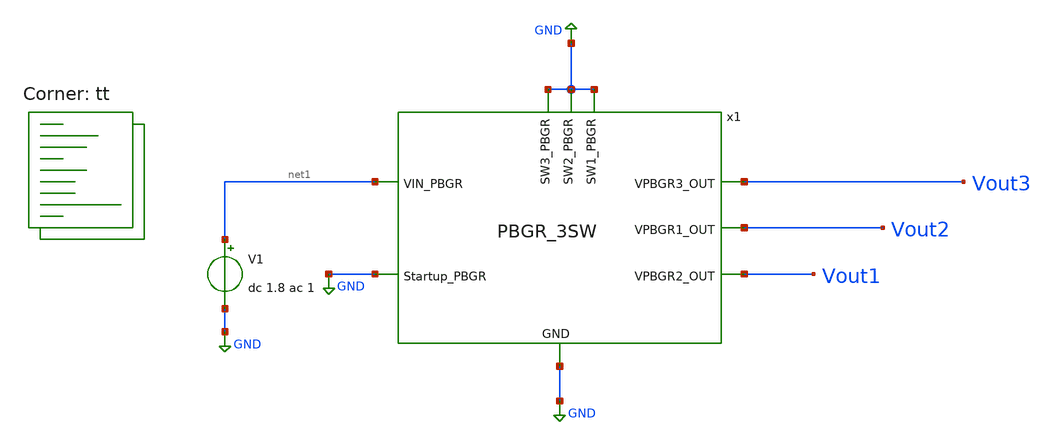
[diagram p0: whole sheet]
** sch_path: PBGR/Three_switch_BGR/tb-try2.sch
**.subckt tb-try2
V1 net1 GND dc 1.8 ac 1
x1 net1 GND Vout3 Vout2 Vout1 GND GND GND GND PBGR_3SW
**** begin user architecture code
.lib $::SKYWATER_MODELS/sky130.lib.spice tt


.option wnflag=1
.option savecurrents
.temp 27
.control
save all
write tb-try2.raw
set appendwrite
op
write tb-try2.raw
dc temp -50 150 1
**ac dec 20 1 1e8
plot v(Vout1) v(Vout2) v(Vout3)
plot v(Vout1)
plot v(Vout2)
plot v(Vout3)
plot vdb(Vout1) vdb(Vout2) vdb(Vout3)
.endc


**** end user architecture code
**.ends

* expanding   symbol:  /foss/designs/Sims-new/PBGR/Final-submission/PBGR_3SW.sym # of pins=9
** sym_path: PBGR/Three_switch_BGR/PBGR_3SW.sym
** sch_path: PBGR/Three_switch_BGR/PBGR_3SW.sch
.subckt PBGR_3SW VIN_PBGR Startup_PBGR VPBGR3_OUT VPBGR1_OUT VPBGR2_OUT SW1_PBGR SW2_PBGR SW3_PBGR
+ GND
*.opin VPBGR3_OUT
*.opin VPBGR2_OUT
*.opin VPBGR1_OUT
*.ipin VIN_PBGR
*.ipin GND
*.ipin Startup_PBGR
*.ipin SW1_PBGR
*.ipin SW2_PBGR
*.ipin SW3_PBGR
XM1 net1 vctrl VIN_PBGR VIN_PBGR sky130_fd_pr__pfet_01v8 L=3 W=6.75 nf=1 ad='int((nf+1)/2) * W/nf * 0.29'
+ as='int((nf+2)/2) * W/nf * 0.29' pd='2*int((nf+1)/2) * (W/nf + 0.29)' ps='2*int((nf+2)/2) * (W/nf + 0.29)'
+ nrd='0.29 / W' nrs='0.29 / W' sa=0 sb=0 sd=0 mult=4 m=4
XM2 minus vb0 net1 VIN_PBGR sky130_fd_pr__pfet_01v8 L=3 W=6.75 nf=1 ad='int((nf+1)/2) * W/nf * 0.29'
+ as='int((nf+2)/2) * W/nf * 0.29' pd='2*int((nf+1)/2) * (W/nf + 0.29)' ps='2*int((nf+2)/2) * (W/nf + 0.29)'
+ nrd='0.29 / W' nrs='0.29 / W' sa=0 sb=0 sd=0 mult=4 m=4
XM3 net2 vctrl VIN_PBGR VIN_PBGR sky130_fd_pr__pfet_01v8 L=3 W=6.75 nf=1 ad='int((nf+1)/2) * W/nf * 0.29'
+ as='int((nf+2)/2) * W/nf * 0.29' pd='2*int((nf+1)/2) * (W/nf + 0.29)' ps='2*int((nf+2)/2) * (W/nf + 0.29)'
+ nrd='0.29 / W' nrs='0.29 / W' sa=0 sb=0 sd=0 mult=4 m=4
XM4 plus vb0 net2 VIN_PBGR sky130_fd_pr__pfet_01v8 L=3 W=6.75 nf=1 ad='int((nf+1)/2) * W/nf * 0.29' as='int((nf+2)/2) * W/nf * 0.29'
+ pd='2*int((nf+1)/2) * (W/nf + 0.29)' ps='2*int((nf+2)/2) * (W/nf + 0.29)' nrd='0.29 / W' nrs='0.29 / W'
+ sa=0 sb=0 sd=0 mult=4 m=4
XR1 net29 plus GND sky130_fd_pr__res_xhigh_po_1p41 L=2.262 mult=1 m=1
XR2 net30 net29 GND sky130_fd_pr__res_xhigh_po_1p41 L=2.262 mult=1 m=1
XR3 net31 net30 GND sky130_fd_pr__res_xhigh_po_1p41 L=2.262 mult=1 m=1
XR4 net3 net31 GND sky130_fd_pr__res_xhigh_po_1p41 L=2.262 mult=1 m=1
XQ1 GND GND net3 sky130_fd_pr__pnp_05v5_W3p40L3p40 m=8
XQ2 GND GND minus sky130_fd_pr__pnp_05v5_W3p40L3p40 m=1
XR5 net32 plus GND sky130_fd_pr__res_xhigh_po_1p41 L=21.11 mult=1 m=1
XR6 net33 net32 GND sky130_fd_pr__res_xhigh_po_1p41 L=21.11 mult=1 m=1
XR7 net34 net33 GND sky130_fd_pr__res_xhigh_po_1p41 L=21.11 mult=1 m=1
XR8 GND net34 GND sky130_fd_pr__res_xhigh_po_1p41 L=21.11 mult=1 m=1
XR9 net35 minus GND sky130_fd_pr__res_xhigh_po_1p41 L=21.11 mult=1 m=1
XR10 net36 net35 GND sky130_fd_pr__res_xhigh_po_1p41 L=21.11 mult=1 m=1
XR11 net37 net36 GND sky130_fd_pr__res_xhigh_po_1p41 L=21.11 mult=1 m=1
XR12 GND net37 GND sky130_fd_pr__res_xhigh_po_1p41 L=21.11 mult=1 m=1
XM7 net4 vctrl VIN_PBGR VIN_PBGR sky130_fd_pr__pfet_01v8 L=3 W=6.75 nf=1 ad='int((nf+1)/2) * W/nf * 0.29'
+ as='int((nf+2)/2) * W/nf * 0.29' pd='2*int((nf+1)/2) * (W/nf + 0.29)' ps='2*int((nf+2)/2) * (W/nf + 0.29)'
+ nrd='0.29 / W' nrs='0.29 / W' sa=0 sb=0 sd=0 mult=4 m=4
XM8 net5 vb0 net4 VIN_PBGR sky130_fd_pr__pfet_01v8 L=3 W=6.75 nf=1 ad='int((nf+1)/2) * W/nf * 0.29' as='int((nf+2)/2) * W/nf * 0.29'
+ pd='2*int((nf+1)/2) * (W/nf + 0.29)' ps='2*int((nf+2)/2) * (W/nf + 0.29)' nrd='0.29 / W' nrs='0.29 / W'
+ sa=0 sb=0 sd=0 mult=4 m=4
XR21 net38 net5 GND sky130_fd_pr__res_xhigh_po_1p41 L=3.7 mult=1 m=1
XM9 net6 net5 GND GND sky130_fd_pr__nfet_01v8_lvt L=0.15 W=1 nf=1 ad='int((nf+1)/2) * W/nf * 0.29' as='int((nf+2)/2) * W/nf * 0.29'
+ pd='2*int((nf+1)/2) * (W/nf + 0.29)' ps='2*int((nf+2)/2) * (W/nf + 0.29)' nrd='0.29 / W' nrs='0.29 / W'
+ sa=0 sb=0 sd=0 mult=1 m=1
XM10 net6 net6 VIN_PBGR VIN_PBGR sky130_fd_pr__pfet_01v8 L=3 W=6.75 nf=1 ad='int((nf+1)/2) * W/nf * 0.29'
+ as='int((nf+2)/2) * W/nf * 0.29' pd='2*int((nf+1)/2) * (W/nf + 0.29)' ps='2*int((nf+2)/2) * (W/nf + 0.29)'
+ nrd='0.29 / W' nrs='0.29 / W' sa=0 sb=0 sd=0 mult=4 m=4
XM11 VPBGR1_OUT net6 VIN_PBGR VIN_PBGR sky130_fd_pr__pfet_01v8 L=3 W=6.75 nf=1 ad='int((nf+1)/2) * W/nf * 0.29'
+ as='int((nf+2)/2) * W/nf * 0.29' pd='2*int((nf+1)/2) * (W/nf + 0.29)' ps='2*int((nf+2)/2) * (W/nf + 0.29)'
+ nrd='0.29 / W' nrs='0.29 / W' sa=0 sb=0 sd=0 mult=4 m=4
XM12 net7 vctrl VIN_PBGR VIN_PBGR sky130_fd_pr__pfet_01v8 L=3 W=6.75 nf=1 ad='int((nf+1)/2) * W/nf * 0.29'
+ as='int((nf+2)/2) * W/nf * 0.29' pd='2*int((nf+1)/2) * (W/nf + 0.29)' ps='2*int((nf+2)/2) * (W/nf + 0.29)'
+ nrd='0.29 / W' nrs='0.29 / W' sa=0 sb=0 sd=0 mult=4 m=4
XM13 VPBGR1_OUT vb0 net7 VIN_PBGR sky130_fd_pr__pfet_01v8 L=3 W=6.75 nf=1 ad='int((nf+1)/2) * W/nf * 0.29'
+ as='int((nf+2)/2) * W/nf * 0.29' pd='2*int((nf+1)/2) * (W/nf + 0.29)' ps='2*int((nf+2)/2) * (W/nf + 0.29)'
+ nrd='0.29 / W' nrs='0.29 / W' sa=0 sb=0 sd=0 mult=4 m=4
XR27 net39 VPBGR1_OUT GND sky130_fd_pr__res_xhigh_po_1p41 L=5.61 mult=1 m=1
XR28 net40 net39 GND sky130_fd_pr__res_xhigh_po_1p41 L=5.61 mult=1 m=1
XR29 net41 net40 GND sky130_fd_pr__res_xhigh_po_1p41 L=5.61 mult=1 m=1
XR30 net42 net41 GND sky130_fd_pr__res_xhigh_po_1p41 L=5.61 mult=1 m=1
XR31 net43 net42 GND sky130_fd_pr__res_xhigh_po_1p41 L=5.61 mult=1 m=1
XR32 net44 net43 GND sky130_fd_pr__res_xhigh_po_1p41 L=5.61 mult=1 m=1
XR33 net45 net44 GND sky130_fd_pr__res_xhigh_po_1p41 L=5.61 mult=1 m=1
XR34 GND net45 GND sky130_fd_pr__res_xhigh_po_1p41 L=5.61 mult=1 m=1
XM14 net8 vctrl VIN_PBGR VIN_PBGR sky130_fd_pr__pfet_01v8 L=3 W=5.4 nf=1 ad='int((nf+1)/2) * W/nf * 0.29'
+ as='int((nf+2)/2) * W/nf * 0.29' pd='2*int((nf+1)/2) * (W/nf + 0.29)' ps='2*int((nf+2)/2) * (W/nf + 0.29)'
+ nrd='0.29 / W' nrs='0.29 / W' sa=0 sb=0 sd=0 mult=1 m=1
XR36 net46 net9 GND sky130_fd_pr__res_xhigh_po_1p41 L=18 mult=1 m=1
XM16 net10 net9 GND GND sky130_fd_pr__nfet_01v8_lvt L=0.15 W=1 nf=1 ad='int((nf+1)/2) * W/nf * 0.29'
+ as='int((nf+2)/2) * W/nf * 0.29' pd='2*int((nf+1)/2) * (W/nf + 0.29)' ps='2*int((nf+2)/2) * (W/nf + 0.29)'
+ nrd='0.29 / W' nrs='0.29 / W' sa=0 sb=0 sd=0 mult=1 m=1
XM17 net10 net10 VIN_PBGR VIN_PBGR sky130_fd_pr__pfet_01v8 L=3 W=6.75 nf=1 ad='int((nf+1)/2) * W/nf * 0.29'
+ as='int((nf+2)/2) * W/nf * 0.29' pd='2*int((nf+1)/2) * (W/nf + 0.29)' ps='2*int((nf+2)/2) * (W/nf + 0.29)'
+ nrd='0.29 / W' nrs='0.29 / W' sa=0 sb=0 sd=0 mult=4 m=4
XM18 VPBGR2_OUT net10 VIN_PBGR VIN_PBGR sky130_fd_pr__pfet_01v8 L=3 W=6.75 nf=1 ad='int((nf+1)/2) * W/nf * 0.29'
+ as='int((nf+2)/2) * W/nf * 0.29' pd='2*int((nf+1)/2) * (W/nf + 0.29)' ps='2*int((nf+2)/2) * (W/nf + 0.29)'
+ nrd='0.29 / W' nrs='0.29 / W' sa=0 sb=0 sd=0 mult=4 m=4
XM19 net11 vctrl VIN_PBGR VIN_PBGR sky130_fd_pr__pfet_01v8 L=3 W=6.75 nf=1 ad='int((nf+1)/2) * W/nf * 0.29'
+ as='int((nf+2)/2) * W/nf * 0.29' pd='2*int((nf+1)/2) * (W/nf + 0.29)' ps='2*int((nf+2)/2) * (W/nf + 0.29)'
+ nrd='0.29 / W' nrs='0.29 / W' sa=0 sb=0 sd=0 mult=4 m=4
XM20 VPBGR2_OUT vb0 net11 VIN_PBGR sky130_fd_pr__pfet_01v8 L=3 W=6.75 nf=1 ad='int((nf+1)/2) * W/nf * 0.29'
+ as='int((nf+2)/2) * W/nf * 0.29' pd='2*int((nf+1)/2) * (W/nf + 0.29)' ps='2*int((nf+2)/2) * (W/nf + 0.29)'
+ nrd='0.29 / W' nrs='0.29 / W' sa=0 sb=0 sd=0 mult=4 m=4
XR41 net47 VPBGR2_OUT GND sky130_fd_pr__res_xhigh_po_1p41 L=5.61 mult=1 m=1
XR42 net48 net47 GND sky130_fd_pr__res_xhigh_po_1p41 L=5.61 mult=1 m=1
XR43 net49 net48 GND sky130_fd_pr__res_xhigh_po_1p41 L=5.61 mult=1 m=1
XR44 net50 net49 GND sky130_fd_pr__res_xhigh_po_1p41 L=5.61 mult=1 m=1
XR45 net51 net50 GND sky130_fd_pr__res_xhigh_po_1p41 L=5.61 mult=1 m=1
XR46 net52 net51 GND sky130_fd_pr__res_xhigh_po_1p41 L=5.61 mult=1 m=1
XR47 net53 net52 GND sky130_fd_pr__res_xhigh_po_1p41 L=5.61 mult=1 m=1
XR48 GND net53 GND sky130_fd_pr__res_xhigh_po_1p41 L=5.61 mult=1 m=1
XR35 net54 net46 GND sky130_fd_pr__res_xhigh_po_1p41 L=18 mult=1 m=1
XR37 GND net55 GND sky130_fd_pr__res_xhigh_po_1p41 L=18 mult=1 m=1
XR38 net55 net54 GND sky130_fd_pr__res_xhigh_po_1p41 L=18 mult=1 m=1
XM15 net9 vb0 net8 VIN_PBGR sky130_fd_pr__pfet_01v8 L=3 W=5.4 nf=1 ad='int((nf+1)/2) * W/nf * 0.29' as='int((nf+2)/2) * W/nf * 0.29'
+ pd='2*int((nf+1)/2) * (W/nf + 0.29)' ps='2*int((nf+2)/2) * (W/nf + 0.29)' nrd='0.29 / W' nrs='0.29 / W'
+ sa=0 sb=0 sd=0 mult=1 m=1
.save v(plus)
.save v(minus)
XM21 vb0 vb0 VIN_PBGR VIN_PBGR sky130_fd_pr__pfet_01v8 L=3 W=6.75 nf=1 ad='int((nf+1)/2) * W/nf * 0.29'
+ as='int((nf+2)/2) * W/nf * 0.29' pd='2*int((nf+1)/2) * (W/nf + 0.29)' ps='2*int((nf+2)/2) * (W/nf + 0.29)'
+ nrd='0.29 / W' nrs='0.29 / W' sa=0 sb=0 sd=0 mult=1 m=1
XR26 net56 vb0 GND sky130_fd_pr__res_xhigh_po_1p41 L=2.9 mult=1 m=1
XR39 net57 net56 GND sky130_fd_pr__res_xhigh_po_1p41 L=2.9 mult=1 m=1
XR40 net58 net57 GND sky130_fd_pr__res_xhigh_po_1p41 L=2.9 mult=1 m=1
XR49 net59 net58 GND sky130_fd_pr__res_xhigh_po_1p41 L=2.9 mult=1 m=1
XR50 net60 net59 GND sky130_fd_pr__res_xhigh_po_1p41 L=2.9 mult=1 m=1
XR51 net61 net60 GND sky130_fd_pr__res_xhigh_po_1p41 L=2.9 mult=1 m=1
XR52 net62 net61 GND sky130_fd_pr__res_xhigh_po_1p41 L=2.9 mult=1 m=1
XR53 GND net62 GND sky130_fd_pr__res_xhigh_po_1p41 L=2.9 mult=1 m=1
XR22 net63 net38 GND sky130_fd_pr__res_xhigh_po_1p41 L=3.7 mult=1 m=1
XR23 GND net64 GND sky130_fd_pr__res_xhigh_po_1p41 L=3.7 mult=1 m=1
XR24 net64 net63 GND sky130_fd_pr__res_xhigh_po_1p41 L=3.7 mult=1 m=1
XM5 net13 minus net12 GND sky130_fd_pr__nfet_01v8_lvt L=1.5 W=2.25 nf=1 ad='int((nf+1)/2) * W/nf * 0.29'
+ as='int((nf+2)/2) * W/nf * 0.29' pd='2*int((nf+1)/2) * (W/nf + 0.29)' ps='2*int((nf+2)/2) * (W/nf + 0.29)'
+ nrd='0.29 / W' nrs='0.29 / W' sa=0 sb=0 sd=0 mult=4 m=4
XM6 net14 plus net12 GND sky130_fd_pr__nfet_01v8_lvt L=1.5 W=2.25 nf=1 ad='int((nf+1)/2) * W/nf * 0.29'
+ as='int((nf+2)/2) * W/nf * 0.29' pd='2*int((nf+1)/2) * (W/nf + 0.29)' ps='2*int((nf+2)/2) * (W/nf + 0.29)'
+ nrd='0.29 / W' nrs='0.29 / W' sa=0 sb=0 sd=0 mult=4 m=4
XM22 net12 net15 GND GND sky130_fd_pr__nfet_01v8 L=2.5 W=2 nf=1 ad='int((nf+1)/2) * W/nf * 0.29' as='int((nf+2)/2) * W/nf * 0.29'
+ pd='2*int((nf+1)/2) * (W/nf + 0.29)' ps='2*int((nf+2)/2) * (W/nf + 0.29)' nrd='0.29 / W' nrs='0.29 / W'
+ sa=0 sb=0 sd=0 mult=4 m=4
XM23 net13 net13 VIN_PBGR VIN_PBGR sky130_fd_pr__pfet_01v8 L=1 W=3 nf=1 ad='int((nf+1)/2) * W/nf * 0.29'
+ as='int((nf+2)/2) * W/nf * 0.29' pd='2*int((nf+1)/2) * (W/nf + 0.29)' ps='2*int((nf+2)/2) * (W/nf + 0.29)'
+ nrd='0.29 / W' nrs='0.29 / W' sa=0 sb=0 sd=0 mult=1 m=1
XM24 net14 net13 VIN_PBGR VIN_PBGR sky130_fd_pr__pfet_01v8 L=1 W=3 nf=1 ad='int((nf+1)/2) * W/nf * 0.29'
+ as='int((nf+2)/2) * W/nf * 0.29' pd='2*int((nf+1)/2) * (W/nf + 0.29)' ps='2*int((nf+2)/2) * (W/nf + 0.29)'
+ nrd='0.29 / W' nrs='0.29 / W' sa=0 sb=0 sd=0 mult=1 m=1
XM25 net15 net15 GND GND sky130_fd_pr__nfet_01v8 L=2.5 W=2 nf=1 ad='int((nf+1)/2) * W/nf * 0.29' as='int((nf+2)/2) * W/nf * 0.29'
+ pd='2*int((nf+1)/2) * (W/nf + 0.29)' ps='2*int((nf+2)/2) * (W/nf + 0.29)' nrd='0.29 / W' nrs='0.29 / W'
+ sa=0 sb=0 sd=0 mult=4 m=4
XR13 net15 net65 GND sky130_fd_pr__res_xhigh_po_1p41 L=9 mult=1 m=1
XR14 net65 net66 GND sky130_fd_pr__res_xhigh_po_1p41 L=9 mult=1 m=1
XR15 net66 net67 GND sky130_fd_pr__res_xhigh_po_1p41 L=9 mult=1 m=1
XR16 net67 net68 GND sky130_fd_pr__res_xhigh_po_1p41 L=9 mult=1 m=1
XR17 net68 net16 GND sky130_fd_pr__res_xhigh_po_1p41 L=9 mult=1 m=1
XR18 net17 net69 GND sky130_fd_pr__res_xhigh_po_1p41 L=9 mult=1 m=1
XR19 net69 net70 GND sky130_fd_pr__res_xhigh_po_1p41 L=9 mult=1 m=1
XR20 net70 net71 GND sky130_fd_pr__res_xhigh_po_1p41 L=9 mult=1 m=1
XR59 net71 net72 GND sky130_fd_pr__res_xhigh_po_1p41 L=9 mult=1 m=1
XR60 net72 net16 GND sky130_fd_pr__res_xhigh_po_1p41 L=9 mult=1 m=1
XR61 net17 net73 GND sky130_fd_pr__res_xhigh_po_1p41 L=9 mult=1 m=1
XR62 net73 net74 GND sky130_fd_pr__res_xhigh_po_1p41 L=9 mult=1 m=1
XR63 net74 net75 GND sky130_fd_pr__res_xhigh_po_1p41 L=9 mult=1 m=1
XR64 net75 net76 GND sky130_fd_pr__res_xhigh_po_1p41 L=9 mult=1 m=1
XR65 net76 net77 GND sky130_fd_pr__res_xhigh_po_1p41 L=9 mult=1 m=1
XR66 net77 VIN_PBGR GND sky130_fd_pr__res_xhigh_po_1p41 L=9 mult=1 m=1
XM26 vctrl net15 GND GND sky130_fd_pr__nfet_01v8 L=2.5 W=8 nf=1 ad='int((nf+1)/2) * W/nf * 0.29' as='int((nf+2)/2) * W/nf * 0.29'
+ pd='2*int((nf+1)/2) * (W/nf + 0.29)' ps='2*int((nf+2)/2) * (W/nf + 0.29)' nrd='0.29 / W' nrs='0.29 / W'
+ sa=0 sb=0 sd=0 mult=4 m=4
XM27 vctrl net14 VIN_PBGR VIN_PBGR sky130_fd_pr__pfet_01v8 L=1 W=4.25 nf=1 ad='int((nf+1)/2) * W/nf * 0.29'
+ as='int((nf+2)/2) * W/nf * 0.29' pd='2*int((nf+1)/2) * (W/nf + 0.29)' ps='2*int((nf+2)/2) * (W/nf + 0.29)'
+ nrd='0.29 / W' nrs='0.29 / W' sa=0 sb=0 sd=0 mult=8 m=8
XR67 net18 vctrl GND sky130_fd_pr__res_xhigh_po_1p41 L=3.5 mult=1 m=1
XC1 net14 net18 sky130_fd_pr__cap_mim_m3_1 W=9.75 L=9.75 MF=8 m=8
XM28 net19 vctrl VIN_PBGR VIN_PBGR sky130_fd_pr__pfet_01v8 L=3 W=6.75 nf=1 ad='int((nf+1)/2) * W/nf * 0.29'
+ as='int((nf+2)/2) * W/nf * 0.29' pd='2*int((nf+1)/2) * (W/nf + 0.29)' ps='2*int((nf+2)/2) * (W/nf + 0.29)'
+ nrd='0.29 / W' nrs='0.29 / W' sa=0 sb=0 sd=0 mult=4 m=4
XM29 net20 vb0 net19 VIN_PBGR sky130_fd_pr__pfet_01v8 L=3 W=6.75 nf=1 ad='int((nf+1)/2) * W/nf * 0.29'
+ as='int((nf+2)/2) * W/nf * 0.29' pd='2*int((nf+1)/2) * (W/nf + 0.29)' ps='2*int((nf+2)/2) * (W/nf + 0.29)'
+ nrd='0.29 / W' nrs='0.29 / W' sa=0 sb=0 sd=0 mult=4 m=4
XR68 net78 net20 GND sky130_fd_pr__res_xhigh_po_1p41 L=4.15 mult=1 m=1
XR69 net79 net78 GND sky130_fd_pr__res_xhigh_po_1p41 L=4.15 mult=1 m=1
XR70 net80 net79 GND sky130_fd_pr__res_xhigh_po_1p41 L=4.15 mult=1 m=1
XR71 GND net80 GND sky130_fd_pr__res_xhigh_po_1p41 L=4.15 mult=1 m=1
XM30 net21 net20 GND GND sky130_fd_pr__nfet_01v8_lvt L=0.15 W=1 nf=1 ad='int((nf+1)/2) * W/nf * 0.29'
+ as='int((nf+2)/2) * W/nf * 0.29' pd='2*int((nf+1)/2) * (W/nf + 0.29)' ps='2*int((nf+2)/2) * (W/nf + 0.29)'
+ nrd='0.29 / W' nrs='0.29 / W' sa=0 sb=0 sd=0 mult=1 m=1
XM31 net21 net21 VIN_PBGR VIN_PBGR sky130_fd_pr__pfet_01v8 L=3 W=6.75 nf=1 ad='int((nf+1)/2) * W/nf * 0.29'
+ as='int((nf+2)/2) * W/nf * 0.29' pd='2*int((nf+1)/2) * (W/nf + 0.29)' ps='2*int((nf+2)/2) * (W/nf + 0.29)'
+ nrd='0.29 / W' nrs='0.29 / W' sa=0 sb=0 sd=0 mult=4 m=4
XM32 VPBGR3_OUT net21 VIN_PBGR VIN_PBGR sky130_fd_pr__pfet_01v8 L=3 W=6.75 nf=1 ad='int((nf+1)/2) * W/nf * 0.29'
+ as='int((nf+2)/2) * W/nf * 0.29' pd='2*int((nf+1)/2) * (W/nf + 0.29)' ps='2*int((nf+2)/2) * (W/nf + 0.29)'
+ nrd='0.29 / W' nrs='0.29 / W' sa=0 sb=0 sd=0 mult=4 m=4
XR74 net23 VPBGR3_OUT GND sky130_fd_pr__res_xhigh_po_1p41 L=5.61 mult=1 m=1
XR75 net81 net23 GND sky130_fd_pr__res_xhigh_po_1p41 L=5.61 mult=1 m=1
XR76 net24 net81 GND sky130_fd_pr__res_xhigh_po_1p41 L=5.61 mult=1 m=1
XR77 net25 net24 GND sky130_fd_pr__res_xhigh_po_1p41 L=5.61 mult=1 m=1
XR78 net82 net25 GND sky130_fd_pr__res_xhigh_po_1p41 L=5.61 mult=1 m=1
XR79 net26 net82 GND sky130_fd_pr__res_xhigh_po_1p41 L=5.61 mult=1 m=1
XR80 net27 net26 GND sky130_fd_pr__res_xhigh_po_1p41 L=5.61 mult=1 m=1
XR81 GND net27 GND sky130_fd_pr__res_xhigh_po_1p41 L=5.61 mult=1 m=1
XM33 VPBGR3_OUT SW1_PBGR net23 GND sky130_fd_pr__nfet_01v8_lvt L=0.15 W=10 nf=1 ad='int((nf+1)/2) * W/nf * 0.29'
+ as='int((nf+2)/2) * W/nf * 0.29' pd='2*int((nf+1)/2) * (W/nf + 0.29)' ps='2*int((nf+2)/2) * (W/nf + 0.29)'
+ nrd='0.29 / W' nrs='0.29 / W' sa=0 sb=0 sd=0 mult=2 m=2
XM34 net22 vctrl VIN_PBGR VIN_PBGR sky130_fd_pr__pfet_01v8 L=3 W=6.75 nf=1 ad='int((nf+1)/2) * W/nf * 0.29'
+ as='int((nf+2)/2) * W/nf * 0.29' pd='2*int((nf+1)/2) * (W/nf + 0.29)' ps='2*int((nf+2)/2) * (W/nf + 0.29)'
+ nrd='0.29 / W' nrs='0.29 / W' sa=0 sb=0 sd=0 mult=4 m=4
XM35 VPBGR3_OUT vb0 net22 VIN_PBGR sky130_fd_pr__pfet_01v8 L=3 W=6.75 nf=1 ad='int((nf+1)/2) * W/nf * 0.29'
+ as='int((nf+2)/2) * W/nf * 0.29' pd='2*int((nf+1)/2) * (W/nf + 0.29)' ps='2*int((nf+2)/2) * (W/nf + 0.29)'
+ nrd='0.29 / W' nrs='0.29 / W' sa=0 sb=0 sd=0 mult=4 m=4
XM37 net24 SW2_PBGR net25 GND sky130_fd_pr__nfet_01v8_lvt L=0.15 W=10 nf=1 ad='int((nf+1)/2) * W/nf * 0.29'
+ as='int((nf+2)/2) * W/nf * 0.29' pd='2*int((nf+1)/2) * (W/nf + 0.29)' ps='2*int((nf+2)/2) * (W/nf + 0.29)'
+ nrd='0.29 / W' nrs='0.29 / W' sa=0 sb=0 sd=0 mult=2 m=2
XM41 net26 SW3_PBGR net27 GND sky130_fd_pr__nfet_01v8_lvt L=0.15 W=10 nf=1 ad='int((nf+1)/2) * W/nf * 0.29'
+ as='int((nf+2)/2) * W/nf * 0.29' pd='2*int((nf+1)/2) * (W/nf + 0.29)' ps='2*int((nf+2)/2) * (W/nf + 0.29)'
+ nrd='0.29 / W' nrs='0.29 / W' sa=0 sb=0 sd=0 mult=2 m=2
XM43 VIN_PBGR VIN_PBGR VIN_PBGR VIN_PBGR sky130_fd_pr__pfet_01v8 L=1 W=3 nf=1 ad='int((nf+1)/2) * W/nf * 0.29'
+ as='int((nf+2)/2) * W/nf * 0.29' pd='2*int((nf+1)/2) * (W/nf + 0.29)' ps='2*int((nf+2)/2) * (W/nf + 0.29)'
+ nrd='0.29 / W' nrs='0.29 / W' sa=0 sb=0 sd=0 mult=6 m=6
XR82 GND GND GND sky130_fd_pr__res_xhigh_po_1p41 L=2.262 mult=1 m=1
XR83 GND GND GND sky130_fd_pr__res_xhigh_po_1p41 L=2.262 mult=1 m=1
XR84 GND GND GND sky130_fd_pr__res_xhigh_po_1p41 L=2.262 mult=1 m=1
XR85 GND GND GND sky130_fd_pr__res_xhigh_po_1p41 L=2.262 mult=1 m=1
XR86 GND GND GND sky130_fd_pr__res_xhigh_po_1p41 L=3.7 mult=1 m=1
XR87 GND GND GND sky130_fd_pr__res_xhigh_po_1p41 L=3.7 mult=1 m=1
XR88 GND GND GND sky130_fd_pr__res_xhigh_po_1p41 L=3.7 mult=1 m=1
XR89 GND GND GND sky130_fd_pr__res_xhigh_po_1p41 L=3.7 mult=1 m=1
XM44 GND GND GND GND sky130_fd_pr__nfet_01v8 L=2.5 W=8 nf=1 ad='int((nf+1)/2) * W/nf * 0.29' as='int((nf+2)/2) * W/nf * 0.29'
+ pd='2*int((nf+1)/2) * (W/nf + 0.29)' ps='2*int((nf+2)/2) * (W/nf + 0.29)' nrd='0.29 / W' nrs='0.29 / W'
+ sa=0 sb=0 sd=0 mult=4 m=4
XR90 GND GND GND sky130_fd_pr__res_xhigh_po_1p41 L=18 mult=1 m=1
XR91 GND GND GND sky130_fd_pr__res_xhigh_po_1p41 L=18 mult=1 m=1
XR92 GND net28 GND sky130_fd_pr__res_xhigh_po_1p41 L=18 mult=1 m=1
XR93 GND net28 GND sky130_fd_pr__res_xhigh_po_1p41 L=18 mult=1 m=1
XR94 GND GND GND sky130_fd_pr__res_xhigh_po_1p41 L=4.15 mult=1 m=1
XR95 GND GND GND sky130_fd_pr__res_xhigh_po_1p41 L=4.15 mult=1 m=1
XR96 GND GND GND sky130_fd_pr__res_xhigh_po_1p41 L=4.15 mult=1 m=1
XR97 GND GND GND sky130_fd_pr__res_xhigh_po_1p41 L=4.15 mult=1 m=1
XM45 vctrl Startup_PBGR GND GND sky130_fd_pr__nfet_01v8_lvt L=0.15 W=1 nf=1 ad='int((nf+1)/2) * W/nf * 0.29'
+ as='int((nf+2)/2) * W/nf * 0.29' pd='2*int((nf+1)/2) * (W/nf + 0.29)' ps='2*int((nf+2)/2) * (W/nf + 0.29)'
+ nrd='0.29 / W' nrs='0.29 / W' sa=0 sb=0 sd=0 mult=1 m=1
.ends

.GLOBAL GND
.end
